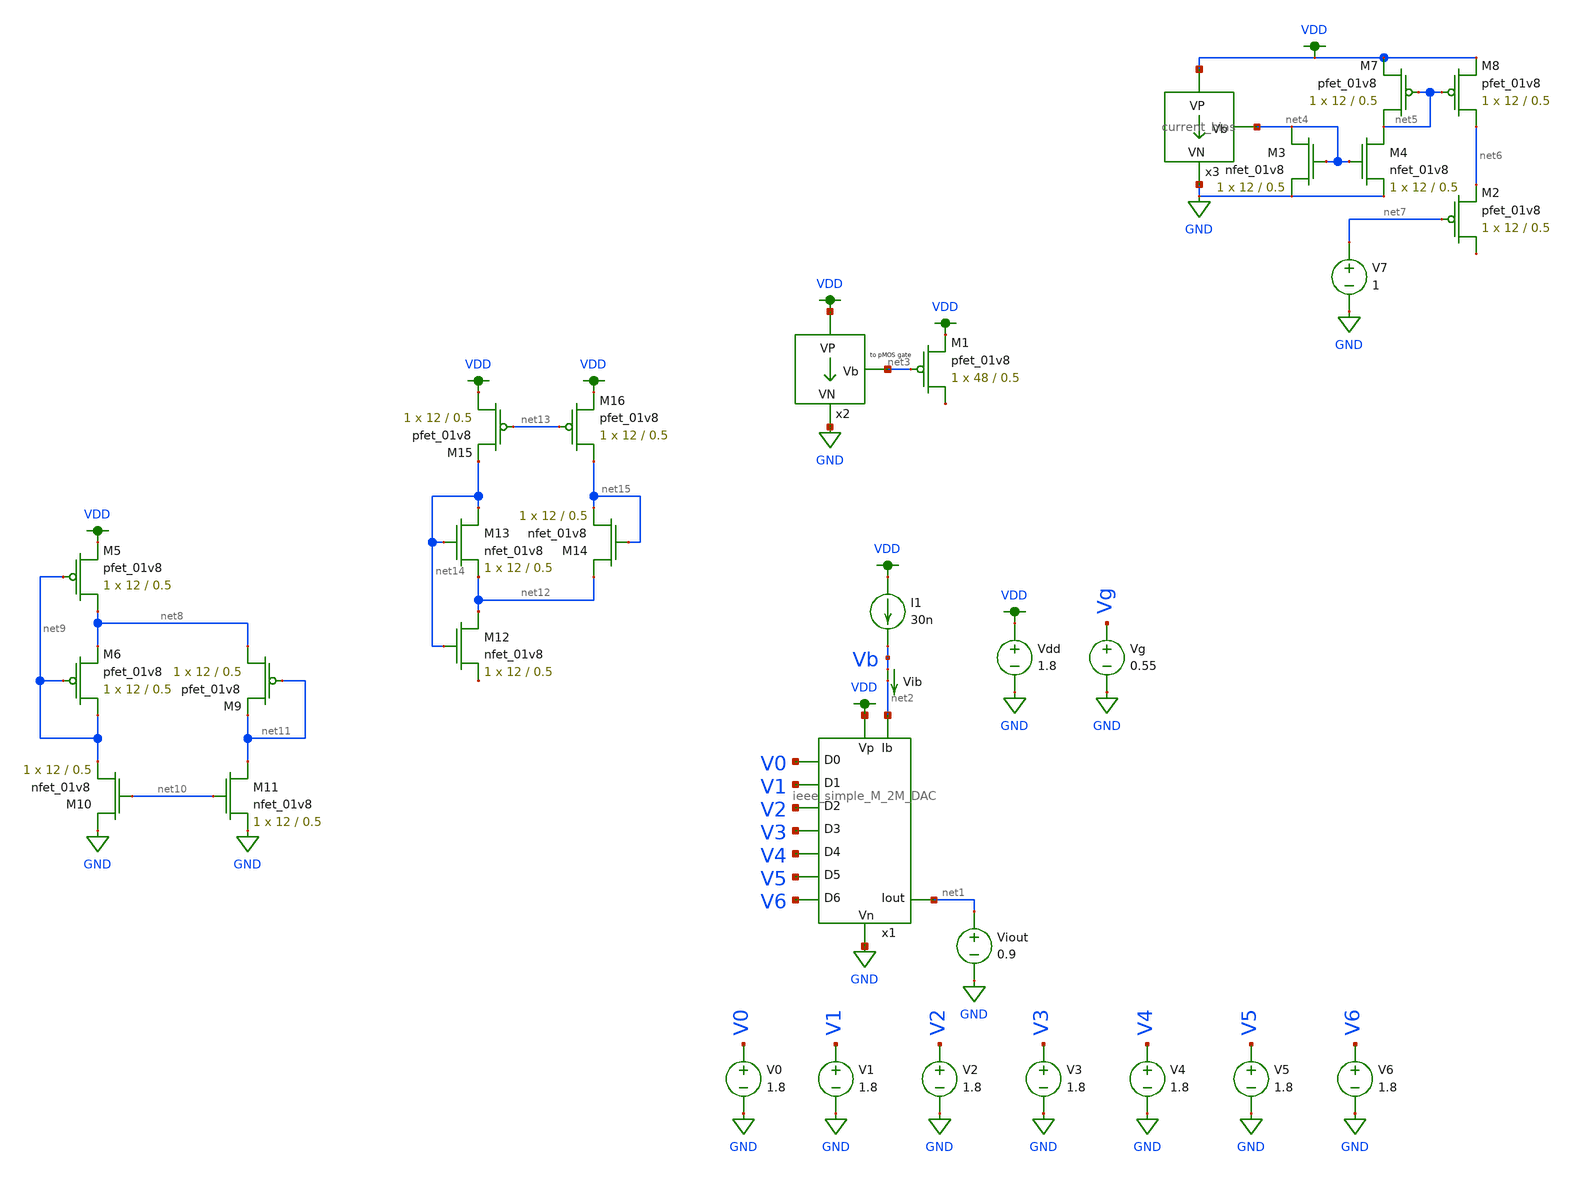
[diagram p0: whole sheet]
** sch_path: schematics/ieee DAC/ieee_DAC_mc_simulation.sch
**.subckt ieee_DAC_mc_simulation
Vdd VDD GND 1.8
V1 V1 GND 1.8
V2 V2 GND 1.8
V3 V3 GND 1.8
V4 V4 GND 1.8
V5 V5 GND 1.8
V6 V6 GND 1.8
V0 V0 GND 1.8
Viout net1 GND 0.9
Vib Vb net2 0
.save i(vib)
x1 VDD net1 GND V1 V0 V2 V3 V4 V5 V6 net2 ieee_simple_M_2M_DAC
XM1 net16 net3 VDD VDD sky130_fd_pr__pfet_01v8 L=0.5 W=48 nf=1 ad='int((nf+1)/2) * W/nf * 0.29' as='int((nf+2)/2) * W/nf * 0.29'
+ pd='2*int((nf+1)/2) * (W/nf + 0.29)' ps='2*int((nf+2)/2) * (W/nf + 0.29)' nrd='0.29 / W' nrs='0.29 / W'
+ sa=0 sb=0 sd=0 mult=1 m=1
x2 VDD net3 GND current_bias
I1 VDD Vb 30n
x3 VDD net4 GND current_bias
XM3 net4 net4 GND GND sky130_fd_pr__nfet_01v8 L=0.5 W=12 nf=1 ad='int((nf+1)/2) * W/nf * 0.29' as='int((nf+2)/2) * W/nf * 0.29'
+ pd='2*int((nf+1)/2) * (W/nf + 0.29)' ps='2*int((nf+2)/2) * (W/nf + 0.29)' nrd='0.29 / W' nrs='0.29 / W'
+ sa=0 sb=0 sd=0 mult=1 m=1
XM4 net5 net4 GND GND sky130_fd_pr__nfet_01v8 L=0.5 W=12 nf=1 ad='int((nf+1)/2) * W/nf * 0.29' as='int((nf+2)/2) * W/nf * 0.29'
+ pd='2*int((nf+1)/2) * (W/nf + 0.29)' ps='2*int((nf+2)/2) * (W/nf + 0.29)' nrd='0.29 / W' nrs='0.29 / W'
+ sa=0 sb=0 sd=0 mult=1 m=1
XM7 net5 net5 VDD VDD sky130_fd_pr__pfet_01v8 L=0.5 W=12 nf=1 ad='int((nf+1)/2) * W/nf * 0.29' as='int((nf+2)/2) * W/nf * 0.29'
+ pd='2*int((nf+1)/2) * (W/nf + 0.29)' ps='2*int((nf+2)/2) * (W/nf + 0.29)' nrd='0.29 / W' nrs='0.29 / W'
+ sa=0 sb=0 sd=0 mult=1 m=1
XM8 net6 net5 VDD VDD sky130_fd_pr__pfet_01v8 L=0.5 W=12 nf=1 ad='int((nf+1)/2) * W/nf * 0.29' as='int((nf+2)/2) * W/nf * 0.29'
+ pd='2*int((nf+1)/2) * (W/nf + 0.29)' ps='2*int((nf+2)/2) * (W/nf + 0.29)' nrd='0.29 / W' nrs='0.29 / W'
+ sa=0 sb=0 sd=0 mult=1 m=1
XM2 net17 net7 net6 VDD sky130_fd_pr__pfet_01v8 L=0.5 W=12 nf=1 ad='int((nf+1)/2) * W/nf * 0.29' as='int((nf+2)/2) * W/nf * 0.29'
+ pd='2*int((nf+1)/2) * (W/nf + 0.29)' ps='2*int((nf+2)/2) * (W/nf + 0.29)' nrd='0.29 / W' nrs='0.29 / W'
+ sa=0 sb=0 sd=0 mult=1 m=1
V7 net7 GND 1
XM5 net8 net9 VDD VDD sky130_fd_pr__pfet_01v8 L=0.5 W=12 nf=1 ad='int((nf+1)/2) * W/nf * 0.29' as='int((nf+2)/2) * W/nf * 0.29'
+ pd='2*int((nf+1)/2) * (W/nf + 0.29)' ps='2*int((nf+2)/2) * (W/nf + 0.29)' nrd='0.29 / W' nrs='0.29 / W'
+ sa=0 sb=0 sd=0 mult=1 m=1
XM6 net9 net9 net8 VDD sky130_fd_pr__pfet_01v8 L=0.5 W=12 nf=1 ad='int((nf+1)/2) * W/nf * 0.29' as='int((nf+2)/2) * W/nf * 0.29'
+ pd='2*int((nf+1)/2) * (W/nf + 0.29)' ps='2*int((nf+2)/2) * (W/nf + 0.29)' nrd='0.29 / W' nrs='0.29 / W'
+ sa=0 sb=0 sd=0 mult=1 m=1
XM9 net8 net11 net11 VDD sky130_fd_pr__pfet_01v8 L=0.5 W=12 nf=1 ad='int((nf+1)/2) * W/nf * 0.29' as='int((nf+2)/2) * W/nf * 0.29'
+ pd='2*int((nf+1)/2) * (W/nf + 0.29)' ps='2*int((nf+2)/2) * (W/nf + 0.29)' nrd='0.29 / W' nrs='0.29 / W'
+ sa=0 sb=0 sd=0 mult=1 m=1
XM10 GND net10 net9 GND sky130_fd_pr__nfet_01v8 L=0.5 W=12 nf=1 ad='int((nf+1)/2) * W/nf * 0.29' as='int((nf+2)/2) * W/nf * 0.29'
+ pd='2*int((nf+1)/2) * (W/nf + 0.29)' ps='2*int((nf+2)/2) * (W/nf + 0.29)' nrd='0.29 / W' nrs='0.29 / W'
+ sa=0 sb=0 sd=0 mult=1 m=1
XM11 net11 net10 GND GND sky130_fd_pr__nfet_01v8 L=0.5 W=12 nf=1 ad='int((nf+1)/2) * W/nf * 0.29' as='int((nf+2)/2) * W/nf * 0.29'
+ pd='2*int((nf+1)/2) * (W/nf + 0.29)' ps='2*int((nf+2)/2) * (W/nf + 0.29)' nrd='0.29 / W' nrs='0.29 / W'
+ sa=0 sb=0 sd=0 mult=1 m=1
Vg Vg GND 0.55
XM12 net12 net14 net18 GND sky130_fd_pr__nfet_01v8 L=0.5 W=12 nf=1 ad='int((nf+1)/2) * W/nf * 0.29' as='int((nf+2)/2) * W/nf * 0.29'
+ pd='2*int((nf+1)/2) * (W/nf + 0.29)' ps='2*int((nf+2)/2) * (W/nf + 0.29)' nrd='0.29 / W' nrs='0.29 / W'
+ sa=0 sb=0 sd=0 mult=1 m=1
XM13 net14 net14 net12 GND sky130_fd_pr__nfet_01v8 L=0.5 W=12 nf=1 ad='int((nf+1)/2) * W/nf * 0.29' as='int((nf+2)/2) * W/nf * 0.29'
+ pd='2*int((nf+1)/2) * (W/nf + 0.29)' ps='2*int((nf+2)/2) * (W/nf + 0.29)' nrd='0.29 / W' nrs='0.29 / W'
+ sa=0 sb=0 sd=0 mult=1 m=1
XM14 net12 net15 net15 GND sky130_fd_pr__nfet_01v8 L=0.5 W=12 nf=1 ad='int((nf+1)/2) * W/nf * 0.29' as='int((nf+2)/2) * W/nf * 0.29'
+ pd='2*int((nf+1)/2) * (W/nf + 0.29)' ps='2*int((nf+2)/2) * (W/nf + 0.29)' nrd='0.29 / W' nrs='0.29 / W'
+ sa=0 sb=0 sd=0 mult=1 m=1
XM15 VDD net13 net14 VDD sky130_fd_pr__pfet_01v8 L=0.5 W=12 nf=1 ad='int((nf+1)/2) * W/nf * 0.29' as='int((nf+2)/2) * W/nf * 0.29'
+ pd='2*int((nf+1)/2) * (W/nf + 0.29)' ps='2*int((nf+2)/2) * (W/nf + 0.29)' nrd='0.29 / W' nrs='0.29 / W'
+ sa=0 sb=0 sd=0 mult=1 m=1
XM16 net15 net13 VDD VDD sky130_fd_pr__pfet_01v8 L=0.5 W=12 nf=1 ad='int((nf+1)/2) * W/nf * 0.29' as='int((nf+2)/2) * W/nf * 0.29'
+ pd='2*int((nf+1)/2) * (W/nf + 0.29)' ps='2*int((nf+2)/2) * (W/nf + 0.29)' nrd='0.29 / W' nrs='0.29 / W'
+ sa=0 sb=0 sd=0 mult=1 m=1
**** begin user architecture code

.option wnflag=1
.param MC_SWITCH=0.0
.lib ~/skywater/skywater-pdk/libraries/sky130_fd_pr_ngspice/latest/models/sky130.lib.spice tt



.control
set wr_vecnames
set wr_singlescale

let Ibias_max = 31n
let Ibias = 30n
dowhile Ibias < Ibias_max
alter Ib $&Ibias

let mc_runs = 1
let run = 1
dowhile run <= mc_runs

  let code = 0
  while code < 128
    if floor(code / 1) eq 0
      let b0 = 0
    else
      let b0 = (floor(code / 1) % 2) * 0.55
    end
    if floor(code / 2) eq 0
      let b1 = 0
    else
      let b1 = (floor(code / 2) % 2) * 0.55
    end
    if floor(code / 4) eq 0
      let b2 = 0
    else
      let b2 = (floor(code / 4) % 2) * 0.55
    end
    if floor(code / 8) eq 0
      let b3 = 0
    else
      let b3 = (floor(code / 8) % 2) * 0.55
    end
    if floor(code / 16) eq 0
      let b4 = 0
    else
      let b4 = (floor(code / 16) % 2) * 0.55
    end
    if floor(code / 32) eq 0
      let b5 = 0
    else
      let b5 = (floor(code / 32) % 2) * 0.55
    end
    if floor(code / 64) eq 0
      let b6 = 0
    else
      let b6 = (floor(code / 64) % 2) * 0.55
    end

    alter V0 $&b0
    alter V1 $&b1
    alter V2 $&b2
    alter V3 $&b3
    alter V4 $&b4
    alter V5 $&b5
    alter V6 $&b6
    save all
    op

    wrdata ~/dev/git/7-bit-D-A-converter-MP4-MADVLSI/schematics/simulations/ieee_DAC/dac_with_external_bias_gen/test_14/ieeeDAC_{$&run}.txt
+ V0 V1 V2 V3 V4 V5 V6 v(Vb) i(Vib) i(Viout)
    if code eq 0
      set appendwrite
      set wr_vecnames = FALSE
    end
    reset
    let code = code + 1
  end

  set appendwrite = FALSE
  set wr_vecnames
  let run = run + 1
end

let Ibias = Ibias * 2
end

quit
.endc

**** end user architecture code
**.ends

* expanding   symbol:  /home/madvlsi/dev/git/7-bit-D-A-converter-MP4-MADVLSI/schematics/ieee
*+ DAC/ieee_simple_M_2M_DAC.sym # of pins=11
** sym_path: mp4_submission/DAC/schematics/ieee_simple_M_2M_DAC.sym
** sch_path: mp4_submission/DAC/schematics/ieee_simple_M_2M_DAC.sch
.subckt ieee_simple_M_2M_DAC VDD Iout GND D1 D0 D2 D3 D4 D5 D6 Ibias
*.ipin Ibias
*.opin Iout
*.ipin D0
*.ipin D1
*.ipin D2
*.ipin D3
*.ipin D4
*.ipin D5
*.ipin D6
*.iopin VDD
*.iopin GND
x1 VDD GND net8 GND inverter
x2 VDD D0 net1 GND inverter
x3 VDD D1 net2 GND inverter
x4 VDD D2 net3 GND inverter
x5 VDD D3 net4 GND inverter
x6 VDD D4 net5 GND inverter
x7 VDD D5 net6 GND inverter
x8 VDD D6 net7 GND inverter
x9 Ibias net8 net1 net3 net4 net5 net6 D5 net2 D0 D1 D2 D3 D4 net7 D6 Iout GND ieee_DAC
.ends


* expanding   symbol:
*+  /home/madvlsi/dev/git/7-bit-D-A-converter-MP4-MADVLSI/schematics/bias_2/current_bias.sym # of pins=3
** sym_path: schematics/bias_2/current_bias.sym
** sch_path: schematics/bias_2/current_bias.sch
.subckt current_bias VP Vb VN
*.iopin VP
*.iopin VN
*.opin Vb
XM4 net1 net1 net4 GND sky130_fd_pr__nfet_01v8 L=0.5 W=12 nf=1 ad='int((nf+1)/2) * W/nf * 0.29' as='int((nf+2)/2) * W/nf * 0.29'
+ pd='2*int((nf+1)/2) * (W/nf + 0.29)' ps='2*int((nf+2)/2) * (W/nf + 0.29)' nrd='0.29 / W' nrs='0.29 / W'
+ sa=0 sb=0 sd=0 mult=8 m=8
XM5 net3 net1 VN GND sky130_fd_pr__nfet_01v8 L=0.5 W=12 nf=1 ad='int((nf+1)/2) * W/nf * 0.29' as='int((nf+2)/2) * W/nf * 0.29'
+ pd='2*int((nf+1)/2) * (W/nf + 0.29)' ps='2*int((nf+2)/2) * (W/nf + 0.29)' nrd='0.29 / W' nrs='0.29 / W'
+ sa=0 sb=0 sd=0 mult=1 m=1
XM6 Vb net2 VN GND sky130_fd_pr__nfet_01v8 L=0.5 W=12 nf=1 ad='int((nf+1)/2) * W/nf * 0.29' as='int((nf+2)/2) * W/nf * 0.29'
+ pd='2*int((nf+1)/2) * (W/nf + 0.29)' ps='2*int((nf+2)/2) * (W/nf + 0.29)' nrd='0.29 / W' nrs='0.29 / W'
+ sa=0 sb=0 sd=0 mult=1 m=1
XM7 net2 net2 VN GND sky130_fd_pr__nfet_01v8 L=0.5 W=12 nf=1 ad='int((nf+1)/2) * W/nf * 0.29' as='int((nf+2)/2) * W/nf * 0.29'
+ pd='2*int((nf+1)/2) * (W/nf + 0.29)' ps='2*int((nf+2)/2) * (W/nf + 0.29)' nrd='0.29 / W' nrs='0.29 / W'
+ sa=0 sb=0 sd=0 mult=1 m=1
R1 net4 VN 100k m=1
XM8 Vb net3 VP VDD sky130_fd_pr__pfet_01v8 L=0.5 W=12 nf=1 ad='int((nf+1)/2) * W/nf * 0.29' as='int((nf+2)/2) * W/nf * 0.29'
+ pd='2*int((nf+1)/2) * (W/nf + 0.29)' ps='2*int((nf+2)/2) * (W/nf + 0.29)' nrd='0.29 / W' nrs='0.29 / W'
+ sa=0 sb=0 sd=0 mult=1 m=1
XM9 net2 Vb VP VDD sky130_fd_pr__pfet_01v8 L=0.5 W=12 nf=1 ad='int((nf+1)/2) * W/nf * 0.29' as='int((nf+2)/2) * W/nf * 0.29'
+ pd='2*int((nf+1)/2) * (W/nf + 0.29)' ps='2*int((nf+2)/2) * (W/nf + 0.29)' nrd='0.29 / W' nrs='0.29 / W'
+ sa=0 sb=0 sd=0 mult=1 m=1
XM10 net3 net3 VP VDD sky130_fd_pr__pfet_01v8 L=0.5 W=12 nf=1 ad='int((nf+1)/2) * W/nf * 0.29' as='int((nf+2)/2) * W/nf * 0.29'
+ pd='2*int((nf+1)/2) * (W/nf + 0.29)' ps='2*int((nf+2)/2) * (W/nf + 0.29)' nrd='0.29 / W' nrs='0.29 / W'
+ sa=0 sb=0 sd=0 mult=1 m=1
XM11 net1 Vb VP VDD sky130_fd_pr__pfet_01v8 L=0.5 W=12 nf=1 ad='int((nf+1)/2) * W/nf * 0.29' as='int((nf+2)/2) * W/nf * 0.29'
+ pd='2*int((nf+1)/2) * (W/nf + 0.29)' ps='2*int((nf+2)/2) * (W/nf + 0.29)' nrd='0.29 / W' nrs='0.29 / W'
+ sa=0 sb=0 sd=0 mult=1 m=1
.ends


* expanding   symbol:  /home/madvlsi/dev/git/7-bit-D-A-converter-MP4-MADVLSI/schematics/ieee
*+ DAC/inverter.sym # of pins=4
** sym_path: schematics/ieee DAC/inverter.sym
** sch_path: schematics/ieee DAC/inverter.sch
.subckt inverter VDD A Y GND
*.ipin A
*.iopin VDD
*.iopin GND
*.opin Y
XM1 Y A GND GND sky130_fd_pr__nfet_01v8 L=0.5 W=12 nf=1 ad='int((nf+1)/2) * W/nf * 0.29' as='int((nf+2)/2) * W/nf * 0.29'
+ pd='2*int((nf+1)/2) * (W/nf + 0.29)' ps='2*int((nf+2)/2) * (W/nf + 0.29)' nrd='0.29 / W' nrs='0.29 / W'
+ sa=0 sb=0 sd=0 mult=1 m=1
XM2 Y A VDD VDD sky130_fd_pr__pfet_01v8 L=0.5 W=12 nf=1 ad='int((nf+1)/2) * W/nf * 0.29' as='int((nf+2)/2) * W/nf * 0.29'
+ pd='2*int((nf+1)/2) * (W/nf + 0.29)' ps='2*int((nf+2)/2) * (W/nf + 0.29)' nrd='0.29 / W' nrs='0.29 / W'
+ sa=0 sb=0 sd=0 mult=1 m=1
.ends


* expanding   symbol:  /home/madvlsi/dev/git/7-bit-D-A-converter-MP4-MADVLSI/schematics/ieee
*+ DAC/ieee_DAC.sym # of pins=18
** sym_path: schematics/ieee DAC/ieee_DAC.sym
** sch_path: schematics/ieee DAC/ieee_DAC.sch
.subckt ieee_DAC Ibias Vg D0 D2 D3 D4 D5 D5b D1 D0b D1b D2b D3b D4b D6 D6b Iout Idump
*.ipin D0
*.ipin D1
*.ipin D2
*.ipin D3
*.ipin D4
*.ipin D5
*.ipin D6
*.ipin D0b
*.ipin D1b
*.ipin D2b
*.ipin D3b
*.ipin D4b
*.ipin D5b
*.ipin D6b
*.iopin Iout
*.iopin Idump
*.iopin Ibias
*.iopin Vg
XM1 Ibias Vg net12 GND sky130_fd_pr__nfet_01v8 L=0.5 W=12 nf=1 ad='int((nf+1)/2) * W/nf * 0.29' as='int((nf+2)/2) * W/nf * 0.29'
+ pd='2*int((nf+1)/2) * (W/nf + 0.29)' ps='2*int((nf+2)/2) * (W/nf + 0.29)' nrd='0.29 / W' nrs='0.29 / W'
+ sa=0 sb=0 sd=0 mult=1 m=1
XM4 Ibias Vg net1 GND sky130_fd_pr__nfet_01v8 L=0.5 W=12 nf=1 ad='int((nf+1)/2) * W/nf * 0.29' as='int((nf+2)/2) * W/nf * 0.29'
+ pd='2*int((nf+1)/2) * (W/nf + 0.29)' ps='2*int((nf+2)/2) * (W/nf + 0.29)' nrd='0.29 / W' nrs='0.29 / W'
+ sa=0 sb=0 sd=0 mult=1 m=1
XM5 net1 Vg net11 GND sky130_fd_pr__nfet_01v8 L=0.5 W=12 nf=1 ad='int((nf+1)/2) * W/nf * 0.29' as='int((nf+2)/2) * W/nf * 0.29'
+ pd='2*int((nf+1)/2) * (W/nf + 0.29)' ps='2*int((nf+2)/2) * (W/nf + 0.29)' nrd='0.29 / W' nrs='0.29 / W'
+ sa=0 sb=0 sd=0 mult=1 m=1
XM8 net1 Vg net2 GND sky130_fd_pr__nfet_01v8 L=0.5 W=12 nf=1 ad='int((nf+1)/2) * W/nf * 0.29' as='int((nf+2)/2) * W/nf * 0.29'
+ pd='2*int((nf+1)/2) * (W/nf + 0.29)' ps='2*int((nf+2)/2) * (W/nf + 0.29)' nrd='0.29 / W' nrs='0.29 / W'
+ sa=0 sb=0 sd=0 mult=1 m=1
XM9 net2 Vg net10 GND sky130_fd_pr__nfet_01v8 L=0.5 W=12 nf=1 ad='int((nf+1)/2) * W/nf * 0.29' as='int((nf+2)/2) * W/nf * 0.29'
+ pd='2*int((nf+1)/2) * (W/nf + 0.29)' ps='2*int((nf+2)/2) * (W/nf + 0.29)' nrd='0.29 / W' nrs='0.29 / W'
+ sa=0 sb=0 sd=0 mult=1 m=1
XM12 net2 Vg net3 GND sky130_fd_pr__nfet_01v8 L=0.5 W=12 nf=1 ad='int((nf+1)/2) * W/nf * 0.29' as='int((nf+2)/2) * W/nf * 0.29'
+ pd='2*int((nf+1)/2) * (W/nf + 0.29)' ps='2*int((nf+2)/2) * (W/nf + 0.29)' nrd='0.29 / W' nrs='0.29 / W'
+ sa=0 sb=0 sd=0 mult=1 m=1
XM13 net3 Vg net9 GND sky130_fd_pr__nfet_01v8 L=0.5 W=12 nf=1 ad='int((nf+1)/2) * W/nf * 0.29' as='int((nf+2)/2) * W/nf * 0.29'
+ pd='2*int((nf+1)/2) * (W/nf + 0.29)' ps='2*int((nf+2)/2) * (W/nf + 0.29)' nrd='0.29 / W' nrs='0.29 / W'
+ sa=0 sb=0 sd=0 mult=1 m=1
XM16 net3 Vg net4 GND sky130_fd_pr__nfet_01v8 L=0.5 W=12 nf=1 ad='int((nf+1)/2) * W/nf * 0.29' as='int((nf+2)/2) * W/nf * 0.29'
+ pd='2*int((nf+1)/2) * (W/nf + 0.29)' ps='2*int((nf+2)/2) * (W/nf + 0.29)' nrd='0.29 / W' nrs='0.29 / W'
+ sa=0 sb=0 sd=0 mult=1 m=1
XM17 net4 Vg net8 GND sky130_fd_pr__nfet_01v8 L=0.5 W=12 nf=1 ad='int((nf+1)/2) * W/nf * 0.29' as='int((nf+2)/2) * W/nf * 0.29'
+ pd='2*int((nf+1)/2) * (W/nf + 0.29)' ps='2*int((nf+2)/2) * (W/nf + 0.29)' nrd='0.29 / W' nrs='0.29 / W'
+ sa=0 sb=0 sd=0 mult=1 m=1
XM7 net4 Vg net5 GND sky130_fd_pr__nfet_01v8 L=0.5 W=12 nf=1 ad='int((nf+1)/2) * W/nf * 0.29' as='int((nf+2)/2) * W/nf * 0.29'
+ pd='2*int((nf+1)/2) * (W/nf + 0.29)' ps='2*int((nf+2)/2) * (W/nf + 0.29)' nrd='0.29 / W' nrs='0.29 / W'
+ sa=0 sb=0 sd=0 mult=1 m=1
XM10 net5 Vg net7 GND sky130_fd_pr__nfet_01v8 L=0.5 W=12 nf=1 ad='int((nf+1)/2) * W/nf * 0.29' as='int((nf+2)/2) * W/nf * 0.29'
+ pd='2*int((nf+1)/2) * (W/nf + 0.29)' ps='2*int((nf+2)/2) * (W/nf + 0.29)' nrd='0.29 / W' nrs='0.29 / W'
+ sa=0 sb=0 sd=0 mult=1 m=1
XM15 net5 Vg net6 GND sky130_fd_pr__nfet_01v8 L=0.5 W=12 nf=1 ad='int((nf+1)/2) * W/nf * 0.29' as='int((nf+2)/2) * W/nf * 0.29'
+ pd='2*int((nf+1)/2) * (W/nf + 0.29)' ps='2*int((nf+2)/2) * (W/nf + 0.29)' nrd='0.29 / W' nrs='0.29 / W'
+ sa=0 sb=0 sd=0 mult=1 m=1
XM18 net6 Vg net13 GND sky130_fd_pr__nfet_01v8 L=0.5 W=12 nf=1 ad='int((nf+1)/2) * W/nf * 0.29' as='int((nf+2)/2) * W/nf * 0.29'
+ pd='2*int((nf+1)/2) * (W/nf + 0.29)' ps='2*int((nf+2)/2) * (W/nf + 0.29)' nrd='0.29 / W' nrs='0.29 / W'
+ sa=0 sb=0 sd=0 mult=1 m=1
XM2 net7 D5 Iout GND sky130_fd_pr__nfet_01v8 L=0.5 W=12 nf=1 ad='int((nf+1)/2) * W/nf * 0.29' as='int((nf+2)/2) * W/nf * 0.29'
+ pd='2*int((nf+1)/2) * (W/nf + 0.29)' ps='2*int((nf+2)/2) * (W/nf + 0.29)' nrd='0.29 / W' nrs='0.29 / W'
+ sa=0 sb=0 sd=0 mult=1 m=1
XM3 Idump D5b net7 GND sky130_fd_pr__nfet_01v8 L=0.5 W=12 nf=1 ad='int((nf+1)/2) * W/nf * 0.29' as='int((nf+2)/2) * W/nf * 0.29'
+ pd='2*int((nf+1)/2) * (W/nf + 0.29)' ps='2*int((nf+2)/2) * (W/nf + 0.29)' nrd='0.29 / W' nrs='0.29 / W'
+ sa=0 sb=0 sd=0 mult=1 m=1
XM6 net8 D4 Iout GND sky130_fd_pr__nfet_01v8 L=0.5 W=12 nf=1 ad='int((nf+1)/2) * W/nf * 0.29' as='int((nf+2)/2) * W/nf * 0.29'
+ pd='2*int((nf+1)/2) * (W/nf + 0.29)' ps='2*int((nf+2)/2) * (W/nf + 0.29)' nrd='0.29 / W' nrs='0.29 / W'
+ sa=0 sb=0 sd=0 mult=1 m=1
XM11 Idump D4b net8 GND sky130_fd_pr__nfet_01v8 L=0.5 W=12 nf=1 ad='int((nf+1)/2) * W/nf * 0.29' as='int((nf+2)/2) * W/nf * 0.29'
+ pd='2*int((nf+1)/2) * (W/nf + 0.29)' ps='2*int((nf+2)/2) * (W/nf + 0.29)' nrd='0.29 / W' nrs='0.29 / W'
+ sa=0 sb=0 sd=0 mult=1 m=1
XM14 net9 D3 Iout GND sky130_fd_pr__nfet_01v8 L=0.5 W=12 nf=1 ad='int((nf+1)/2) * W/nf * 0.29' as='int((nf+2)/2) * W/nf * 0.29'
+ pd='2*int((nf+1)/2) * (W/nf + 0.29)' ps='2*int((nf+2)/2) * (W/nf + 0.29)' nrd='0.29 / W' nrs='0.29 / W'
+ sa=0 sb=0 sd=0 mult=1 m=1
XM19 Idump D3b net9 GND sky130_fd_pr__nfet_01v8 L=0.5 W=12 nf=1 ad='int((nf+1)/2) * W/nf * 0.29' as='int((nf+2)/2) * W/nf * 0.29'
+ pd='2*int((nf+1)/2) * (W/nf + 0.29)' ps='2*int((nf+2)/2) * (W/nf + 0.29)' nrd='0.29 / W' nrs='0.29 / W'
+ sa=0 sb=0 sd=0 mult=1 m=1
XM20 net10 D2 Iout GND sky130_fd_pr__nfet_01v8 L=0.5 W=12 nf=1 ad='int((nf+1)/2) * W/nf * 0.29' as='int((nf+2)/2) * W/nf * 0.29'
+ pd='2*int((nf+1)/2) * (W/nf + 0.29)' ps='2*int((nf+2)/2) * (W/nf + 0.29)' nrd='0.29 / W' nrs='0.29 / W'
+ sa=0 sb=0 sd=0 mult=1 m=1
XM21 Idump D2b net10 GND sky130_fd_pr__nfet_01v8 L=0.5 W=12 nf=1 ad='int((nf+1)/2) * W/nf * 0.29' as='int((nf+2)/2) * W/nf * 0.29'
+ pd='2*int((nf+1)/2) * (W/nf + 0.29)' ps='2*int((nf+2)/2) * (W/nf + 0.29)' nrd='0.29 / W' nrs='0.29 / W'
+ sa=0 sb=0 sd=0 mult=1 m=1
XM22 net11 D1 Iout GND sky130_fd_pr__nfet_01v8 L=0.5 W=12 nf=1 ad='int((nf+1)/2) * W/nf * 0.29' as='int((nf+2)/2) * W/nf * 0.29'
+ pd='2*int((nf+1)/2) * (W/nf + 0.29)' ps='2*int((nf+2)/2) * (W/nf + 0.29)' nrd='0.29 / W' nrs='0.29 / W'
+ sa=0 sb=0 sd=0 mult=1 m=1
XM23 Idump D1b net11 GND sky130_fd_pr__nfet_01v8 L=0.5 W=12 nf=1 ad='int((nf+1)/2) * W/nf * 0.29' as='int((nf+2)/2) * W/nf * 0.29'
+ pd='2*int((nf+1)/2) * (W/nf + 0.29)' ps='2*int((nf+2)/2) * (W/nf + 0.29)' nrd='0.29 / W' nrs='0.29 / W'
+ sa=0 sb=0 sd=0 mult=1 m=1
XM24 net12 D0 Iout GND sky130_fd_pr__nfet_01v8 L=0.5 W=12 nf=1 ad='int((nf+1)/2) * W/nf * 0.29' as='int((nf+2)/2) * W/nf * 0.29'
+ pd='2*int((nf+1)/2) * (W/nf + 0.29)' ps='2*int((nf+2)/2) * (W/nf + 0.29)' nrd='0.29 / W' nrs='0.29 / W'
+ sa=0 sb=0 sd=0 mult=1 m=1
XM25 Idump D0b net12 GND sky130_fd_pr__nfet_01v8 L=0.5 W=12 nf=1 ad='int((nf+1)/2) * W/nf * 0.29' as='int((nf+2)/2) * W/nf * 0.29'
+ pd='2*int((nf+1)/2) * (W/nf + 0.29)' ps='2*int((nf+2)/2) * (W/nf + 0.29)' nrd='0.29 / W' nrs='0.29 / W'
+ sa=0 sb=0 sd=0 mult=1 m=1
XM26 net13 D6 Iout GND sky130_fd_pr__nfet_01v8 L=0.5 W=12 nf=1 ad='int((nf+1)/2) * W/nf * 0.29' as='int((nf+2)/2) * W/nf * 0.29'
+ pd='2*int((nf+1)/2) * (W/nf + 0.29)' ps='2*int((nf+2)/2) * (W/nf + 0.29)' nrd='0.29 / W' nrs='0.29 / W'
+ sa=0 sb=0 sd=0 mult=1 m=1
XM27 Idump D6b net13 GND sky130_fd_pr__nfet_01v8 L=0.5 W=12 nf=1 ad='int((nf+1)/2) * W/nf * 0.29' as='int((nf+2)/2) * W/nf * 0.29'
+ pd='2*int((nf+1)/2) * (W/nf + 0.29)' ps='2*int((nf+2)/2) * (W/nf + 0.29)' nrd='0.29 / W' nrs='0.29 / W'
+ sa=0 sb=0 sd=0 mult=1 m=1
XM28 net6 Vg net14 GND sky130_fd_pr__nfet_01v8 L=0.5 W=12 nf=1 ad='int((nf+1)/2) * W/nf * 0.29' as='int((nf+2)/2) * W/nf * 0.29'
+ pd='2*int((nf+1)/2) * (W/nf + 0.29)' ps='2*int((nf+2)/2) * (W/nf + 0.29)' nrd='0.29 / W' nrs='0.29 / W'
+ sa=0 sb=0 sd=0 mult=1 m=1
XM29 net14 Vg Idump GND sky130_fd_pr__nfet_01v8 L=0.5 W=12 nf=1 ad='int((nf+1)/2) * W/nf * 0.29' as='int((nf+2)/2) * W/nf * 0.29'
+ pd='2*int((nf+1)/2) * (W/nf + 0.29)' ps='2*int((nf+2)/2) * (W/nf + 0.29)' nrd='0.29 / W' nrs='0.29 / W'
+ sa=0 sb=0 sd=0 mult=1 m=1
.ends

.GLOBAL VDD
.GLOBAL GND
.end
